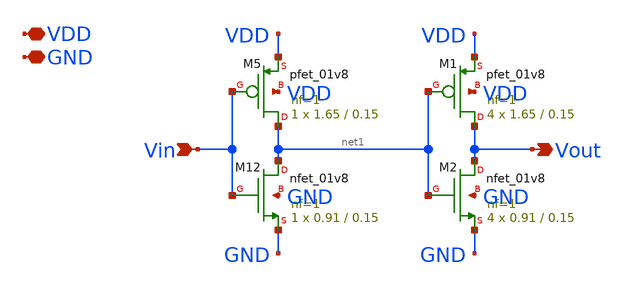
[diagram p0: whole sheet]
** sch_path: xschem/capswitch4/capswitch4.sch
**.subckt capswitch4 Vin Vout VDD GND
*.ipin Vin
*.opin Vout
*.iopin VDD
*.iopin GND
XM5 net1 Vin VDD VDD sky130_fd_pr__pfet_01v8 L=0.15 W=1.65 nf=1 ad='int((nf+1)/2) * W/nf * 0.29' as='int((nf+2)/2) * W/nf * 0.29'
+ pd='2*int((nf+1)/2) * (W/nf + 0.29)' ps='2*int((nf+2)/2) * (W/nf + 0.29)' nrd='0.29 / W' nrs='0.29 / W'
+ sa=0 sb=0 sd=0 mult=1 m=1
XM12 net1 Vin GND GND sky130_fd_pr__nfet_01v8 L=0.15 W=0.91 nf=1 ad='int((nf+1)/2) * W/nf * 0.29' as='int((nf+2)/2) * W/nf * 0.29'
+ pd='2*int((nf+1)/2) * (W/nf + 0.29)' ps='2*int((nf+2)/2) * (W/nf + 0.29)' nrd='0.29 / W' nrs='0.29 / W'
+ sa=0 sb=0 sd=0 mult=1 m=1
XM1 Vout net1 VDD VDD sky130_fd_pr__pfet_01v8 L=0.15 W=1.65 nf=1 ad='int((nf+1)/2) * W/nf * 0.29' as='int((nf+2)/2) * W/nf * 0.29'
+ pd='2*int((nf+1)/2) * (W/nf + 0.29)' ps='2*int((nf+2)/2) * (W/nf + 0.29)' nrd='0.29 / W' nrs='0.29 / W'
+ sa=0 sb=0 sd=0 mult=4 m=4
XM2 Vout net1 GND GND sky130_fd_pr__nfet_01v8 L=0.15 W=0.91 nf=1 ad='int((nf+1)/2) * W/nf * 0.29' as='int((nf+2)/2) * W/nf * 0.29'
+ pd='2*int((nf+1)/2) * (W/nf + 0.29)' ps='2*int((nf+2)/2) * (W/nf + 0.29)' nrd='0.29 / W' nrs='0.29 / W'
+ sa=0 sb=0 sd=0 mult=4 m=4
**.ends
.end
